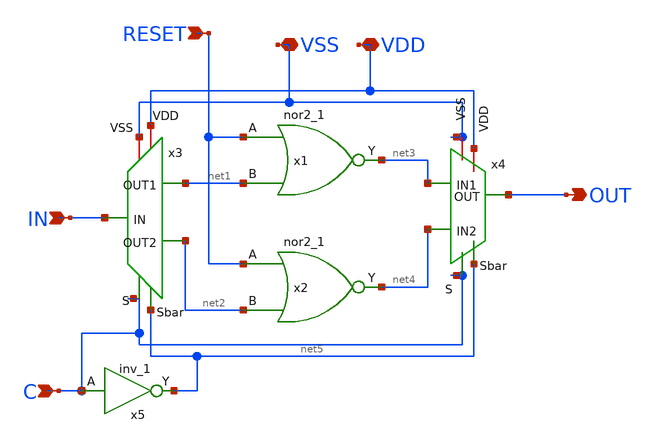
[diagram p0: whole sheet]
** sch_path: xiaolin/singlestage.sch
**.subckt singlestage IN C RESET VSS VDD OUT
*.ipin IN
*.ipin C
*.ipin RESET
*.iopin VSS
*.iopin VDD
*.opin OUT
x1 RESET net1 GND GND VDD VDD net3 sky130_fd_sc_hd__nor2_1
x2 RESET net2 GND GND VDD VDD net4 sky130_fd_sc_hd__nor2_1
x3 C VSS net1 VDD IN net5 net2 demux2-1
x4 C VSS net3 VDD OUT net5 net4 mux2-1
x5 C GND GND VDD VDD net5 sky130_fd_sc_hd__inv_1
**.ends

* expanding   symbol:  demux2-1.sym # of pins=7
** sym_path: xiaolin/demux2-1.sym
** sch_path: xiaolin/demux2-1.sch
.subckt demux2-1 S VSS OUT1 VDD IN Sbar OUT2
*.ipin Sbar
*.ipin S
*.iopin VSS
*.iopin VDD
*.opin OUT1
*.opin OUT2
*.ipin IN
XM2 IN S OUT1 VSS sky130_fd_pr__nfet_01v8 L=0.15 W=0.65 nf=1 ad='int((nf+1)/2) * W/nf * 0.29' as='int((nf+2)/2) * W/nf * 0.29'
+ pd='2*int((nf+1)/2) * (W/nf + 0.29)' ps='2*int((nf+2)/2) * (W/nf + 0.29)' nrd='0.29 / W' nrs='0.29 / W'
+ sa=0 sb=0 sd=0 mult=1 m=1
XM1 IN Sbar OUT2 VSS sky130_fd_pr__nfet_01v8 L=0.15 W=0.65 nf=1 ad='int((nf+1)/2) * W/nf * 0.29' as='int((nf+2)/2) * W/nf * 0.29'
+ pd='2*int((nf+1)/2) * (W/nf + 0.29)' ps='2*int((nf+2)/2) * (W/nf + 0.29)' nrd='0.29 / W' nrs='0.29 / W'
+ sa=0 sb=0 sd=0 mult=1 m=1
XM3 IN S OUT2 VDD sky130_fd_pr__pfet_01v8_hvt L=0.15 W=1 nf=1 ad='int((nf+1)/2) * W/nf * 0.29' as='int((nf+2)/2) * W/nf * 0.29'
+ pd='2*int((nf+1)/2) * (W/nf + 0.29)' ps='2*int((nf+2)/2) * (W/nf + 0.29)' nrd='0.29 / W' nrs='0.29 / W'
+ sa=0 sb=0 sd=0 mult=1 m=1
XM4 IN Sbar OUT1 VDD sky130_fd_pr__pfet_01v8_hvt L=0.15 W=1 nf=1 ad='int((nf+1)/2) * W/nf * 0.29' as='int((nf+2)/2) * W/nf * 0.29'
+ pd='2*int((nf+1)/2) * (W/nf + 0.29)' ps='2*int((nf+2)/2) * (W/nf + 0.29)' nrd='0.29 / W' nrs='0.29 / W'
+ sa=0 sb=0 sd=0 mult=1 m=1
XM5 IN S OUT2 VDD sky130_fd_pr__pfet_01v8_hvt L=0.15 W=1 nf=1 ad='int((nf+1)/2) * W/nf * 0.29' as='int((nf+2)/2) * W/nf * 0.29'
+ pd='2*int((nf+1)/2) * (W/nf + 0.29)' ps='2*int((nf+2)/2) * (W/nf + 0.29)' nrd='0.29 / W' nrs='0.29 / W'
+ sa=0 sb=0 sd=0 mult=1 m=1
.ends


* expanding   symbol:  mux2-1.sym # of pins=7
** sym_path: design/mux2-1.sym
** sch_path: design/mux2-1.sch
.subckt mux2-1 S VSS IN1 VDD OUT Sbar IN2
*.ipin IN1
*.ipin IN2
*.ipin Sbar
*.ipin S
*.opin OUT
*.iopin VSS
*.iopin VDD
XM2 IN1 S OUT VSS sky130_fd_pr__nfet_01v8 L=0.15 W=0.65 nf=1 ad='int((nf+1)/2) * W/nf * 0.29' as='int((nf+2)/2) * W/nf * 0.29'
+ pd='2*int((nf+1)/2) * (W/nf + 0.29)' ps='2*int((nf+2)/2) * (W/nf + 0.29)' nrd='0.29 / W' nrs='0.29 / W'
+ sa=0 sb=0 sd=0 mult=1 m=1
XM1 IN2 Sbar OUT VSS sky130_fd_pr__nfet_01v8 L=0.15 W=0.65 nf=1 ad='int((nf+1)/2) * W/nf * 0.29' as='int((nf+2)/2) * W/nf * 0.29'
+ pd='2*int((nf+1)/2) * (W/nf + 0.29)' ps='2*int((nf+2)/2) * (W/nf + 0.29)' nrd='0.29 / W' nrs='0.29 / W'
+ sa=0 sb=0 sd=0 mult=1 m=1
XM4 IN1 Sbar OUT VDD sky130_fd_pr__pfet_01v8_hvt L=0.15 W=1 nf=1 ad='int((nf+1)/2) * W/nf * 0.29' as='int((nf+2)/2) * W/nf * 0.29'
+ pd='2*int((nf+1)/2) * (W/nf + 0.29)' ps='2*int((nf+2)/2) * (W/nf + 0.29)' nrd='0.29 / W' nrs='0.29 / W'
+ sa=0 sb=0 sd=0 mult=1 m=1
XM5 IN2 S OUT VDD sky130_fd_pr__pfet_01v8_hvt L=0.15 W=1 nf=1 ad='int((nf+1)/2) * W/nf * 0.29' as='int((nf+2)/2) * W/nf * 0.29'
+ pd='2*int((nf+1)/2) * (W/nf + 0.29)' ps='2*int((nf+2)/2) * (W/nf + 0.29)' nrd='0.29 / W' nrs='0.29 / W'
+ sa=0 sb=0 sd=0 mult=1 m=1
.ends

.end
